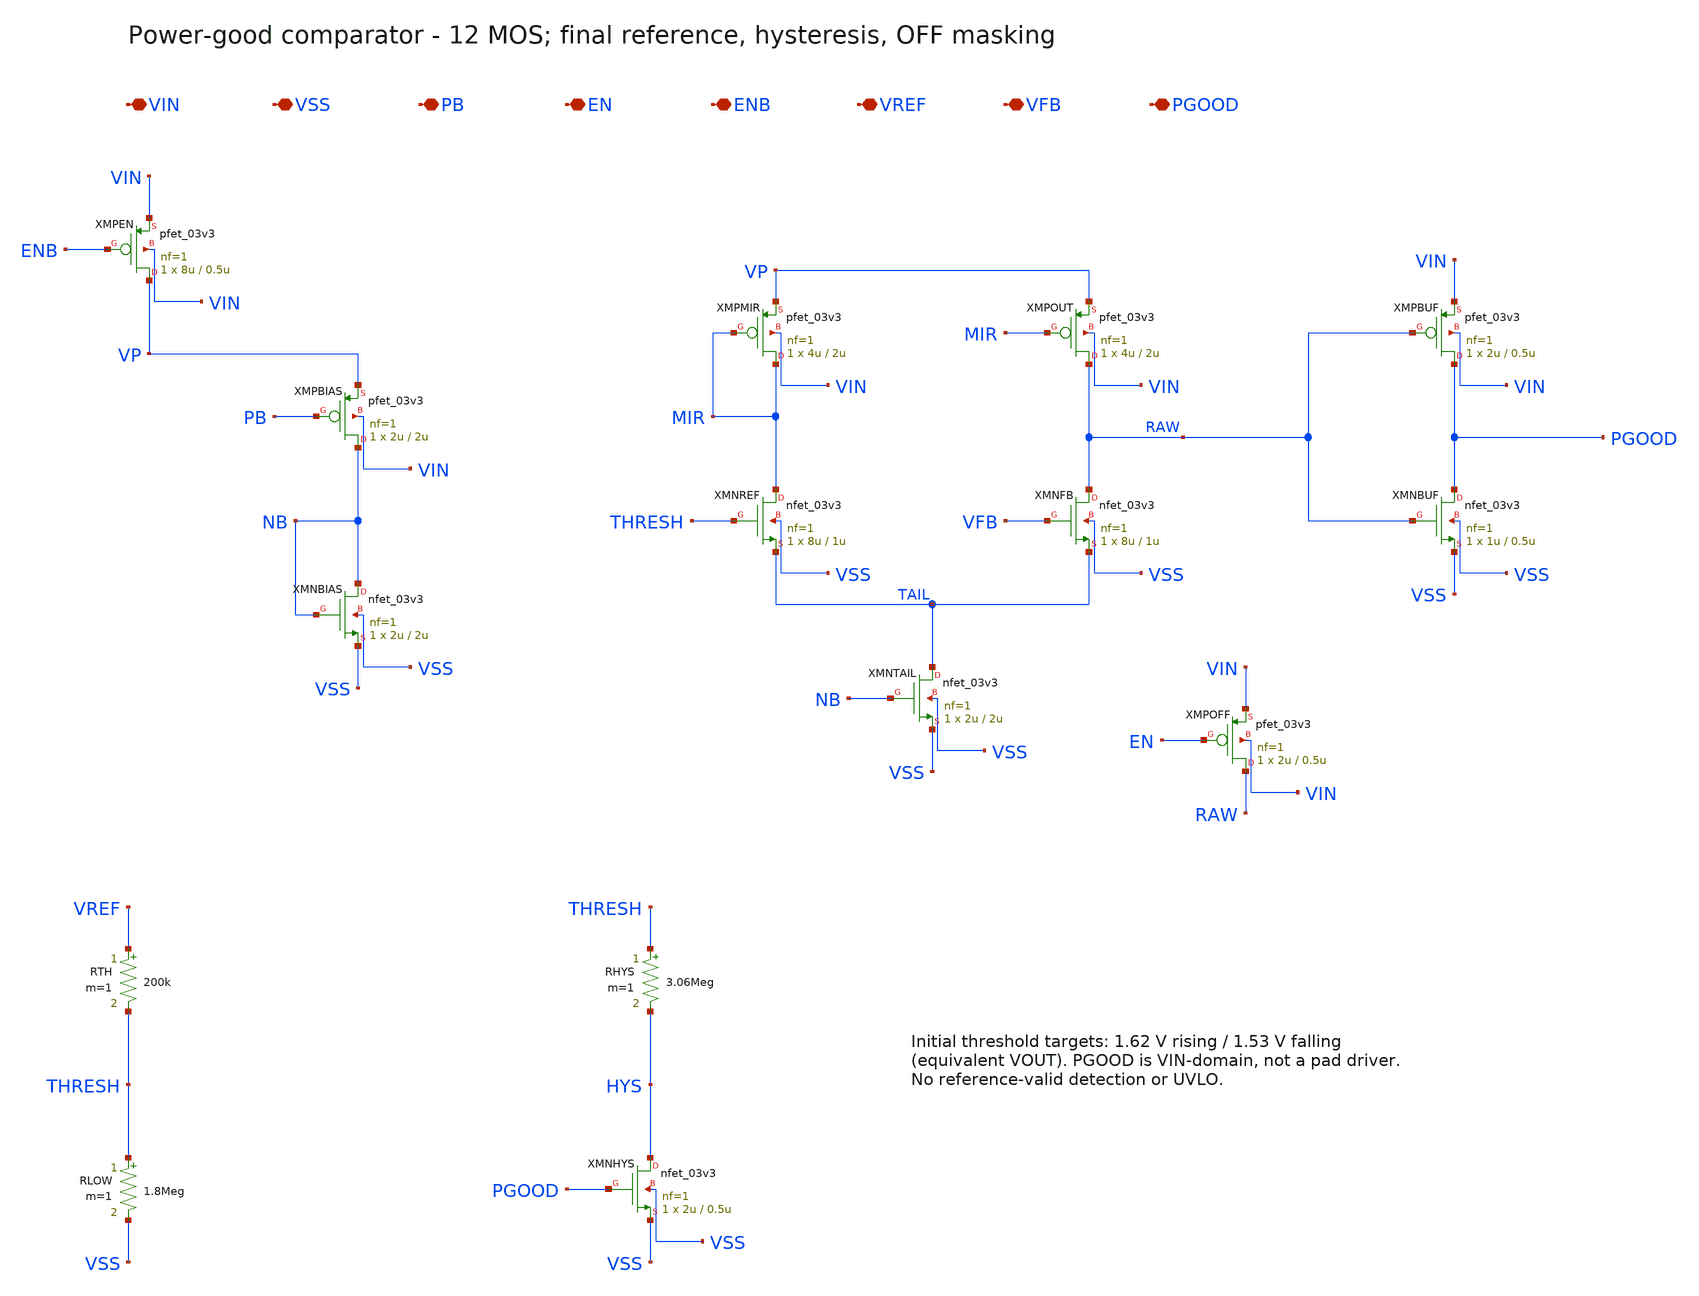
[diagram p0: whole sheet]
** sch_path: schematics/ldo_pgood.sch
**.subckt ldo_pgood VIN VSS PB EN ENB VREF VFB PGOOD
*.iopin VIN
*.iopin VSS
*.iopin PB
*.iopin EN
*.iopin ENB
*.iopin VREF
*.iopin VFB
*.iopin PGOOD
XMPEN VP ENB VIN VIN pfet_03v3 L=0.5u W=8u nf=1 ad='int((nf+1)/2)*W/nf*0.18u' as='int((nf+2)/2)*W/nf*0.18u'
+ pd='2*int((nf+1)/2)*(W/nf+0.18u)' ps='2*int((nf+2)/2)*(W/nf+0.18u)' nrd='0.18u/W' nrs='0.18u/W' sa=0
+ sb=0 sd=0 m=1 par=1
XMPBIAS NB PB VP VIN pfet_03v3 L=2u W=2u nf=1 ad='int((nf+1)/2)*W/nf*0.18u' as='int((nf+2)/2)*W/nf*0.18u'
+ pd='2*int((nf+1)/2)*(W/nf+0.18u)' ps='2*int((nf+2)/2)*(W/nf+0.18u)' nrd='0.18u/W' nrs='0.18u/W' sa=0
+ sb=0 sd=0 m=1 par=1
XMNBIAS NB NB VSS VSS nfet_03v3 L=2u W=2u nf=1 ad='int((nf+1)/2)*W/nf*0.18u' as='int((nf+2)/2)*W/nf*0.18u'
+ pd='2*int((nf+1)/2)*(W/nf+0.18u)' ps='2*int((nf+2)/2)*(W/nf+0.18u)' nrd='0.18u/W' nrs='0.18u/W' sa=0
+ sb=0 sd=0 m=1 par=1
XMPMIR MIR MIR VP VIN pfet_03v3 L=2u W=4u nf=1 ad='int((nf+1)/2)*W/nf*0.18u' as='int((nf+2)/2)*W/nf*0.18u'
+ pd='2*int((nf+1)/2)*(W/nf+0.18u)' ps='2*int((nf+2)/2)*(W/nf+0.18u)' nrd='0.18u/W' nrs='0.18u/W' sa=0
+ sb=0 sd=0 m=1 par=1
XMPOUT RAW MIR VP VIN pfet_03v3 L=2u W=4u nf=1 ad='int((nf+1)/2)*W/nf*0.18u' as='int((nf+2)/2)*W/nf*0.18u'
+ pd='2*int((nf+1)/2)*(W/nf+0.18u)' ps='2*int((nf+2)/2)*(W/nf+0.18u)' nrd='0.18u/W' nrs='0.18u/W' sa=0
+ sb=0 sd=0 m=1 par=1
XMNREF MIR THRESH TAIL VSS nfet_03v3 L=1u W=8u nf=1 ad='int((nf+1)/2)*W/nf*0.18u' as='int((nf+2)/2)*W/nf*0.18u'
+ pd='2*int((nf+1)/2)*(W/nf+0.18u)' ps='2*int((nf+2)/2)*(W/nf+0.18u)' nrd='0.18u/W' nrs='0.18u/W' sa=0
+ sb=0 sd=0 m=1 par=1
XMNFB RAW VFB TAIL VSS nfet_03v3 L=1u W=8u nf=1 ad='int((nf+1)/2)*W/nf*0.18u' as='int((nf+2)/2)*W/nf*0.18u'
+ pd='2*int((nf+1)/2)*(W/nf+0.18u)' ps='2*int((nf+2)/2)*(W/nf+0.18u)' nrd='0.18u/W' nrs='0.18u/W' sa=0
+ sb=0 sd=0 m=1 par=1
XMNTAIL TAIL NB VSS VSS nfet_03v3 L=2u W=2u nf=1 ad='int((nf+1)/2)*W/nf*0.18u' as='int((nf+2)/2)*W/nf*0.18u'
+ pd='2*int((nf+1)/2)*(W/nf+0.18u)' ps='2*int((nf+2)/2)*(W/nf+0.18u)' nrd='0.18u/W' nrs='0.18u/W' sa=0
+ sb=0 sd=0 m=1 par=1
XMPBUF PGOOD RAW VIN VIN pfet_03v3 L=0.5u W=2u nf=1 ad='int((nf+1)/2)*W/nf*0.18u' as='int((nf+2)/2)*W/nf*0.18u'
+ pd='2*int((nf+1)/2)*(W/nf+0.18u)' ps='2*int((nf+2)/2)*(W/nf+0.18u)' nrd='0.18u/W' nrs='0.18u/W' sa=0
+ sb=0 sd=0 m=1 par=1
XMNBUF PGOOD RAW VSS VSS nfet_03v3 L=0.5u W=1u nf=1 ad='int((nf+1)/2)*W/nf*0.18u' as='int((nf+2)/2)*W/nf*0.18u'
+ pd='2*int((nf+1)/2)*(W/nf+0.18u)' ps='2*int((nf+2)/2)*(W/nf+0.18u)' nrd='0.18u/W' nrs='0.18u/W' sa=0
+ sb=0 sd=0 m=1 par=1
XMPOFF RAW EN VIN VIN pfet_03v3 L=0.5u W=2u nf=1 ad='int((nf+1)/2)*W/nf*0.18u' as='int((nf+2)/2)*W/nf*0.18u'
+ pd='2*int((nf+1)/2)*(W/nf+0.18u)' ps='2*int((nf+2)/2)*(W/nf+0.18u)' nrd='0.18u/W' nrs='0.18u/W' sa=0
+ sb=0 sd=0 m=1 par=1
RTH VREF THRESH 200k m=1
RLOW THRESH VSS 1.8Meg m=1
RHYS THRESH HYS 3.06Meg m=1
XMNHYS HYS PGOOD VSS VSS nfet_03v3 L=0.5u W=2u nf=1 ad='int((nf+1)/2)*W/nf*0.18u' as='int((nf+2)/2)*W/nf*0.18u'
+ pd='2*int((nf+1)/2)*(W/nf+0.18u)' ps='2*int((nf+2)/2)*(W/nf+0.18u)' nrd='0.18u/W' nrs='0.18u/W' sa=0
+ sb=0 sd=0 m=1 par=1
**.ends
.end
